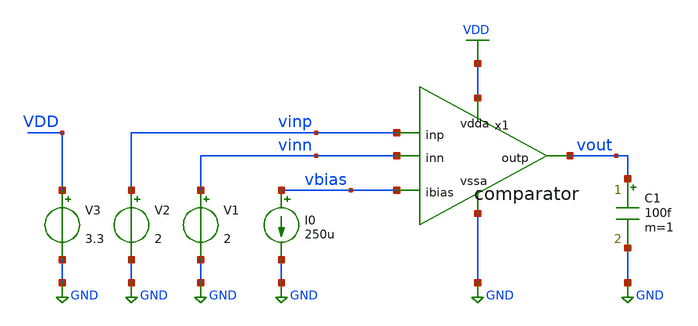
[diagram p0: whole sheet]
** sch_path: xschem/tb_comp_op.sch
**.subckt tb_comp_op
I0 vbias GND 250u
C1 vout GND 100f m=1
V1 vinn GND 2
V3 VDD GND 3.3
V2 vinp GND 2
x1 VDD vbias vinp vinn vout GND comparator
**** begin user architecture code



.lib /home/ttuser/pdk/sky130A/libs.tech/ngspice/sky130.lib.spice tt

.option savecurrents
.save all

.control
optran 0 0 0 10n 10u 0
op
write tb_comp_op.raw
*exit
.endc



**** end user architecture code
**.ends
.GLOBAL GND
.GLOBAL VDD
.end
